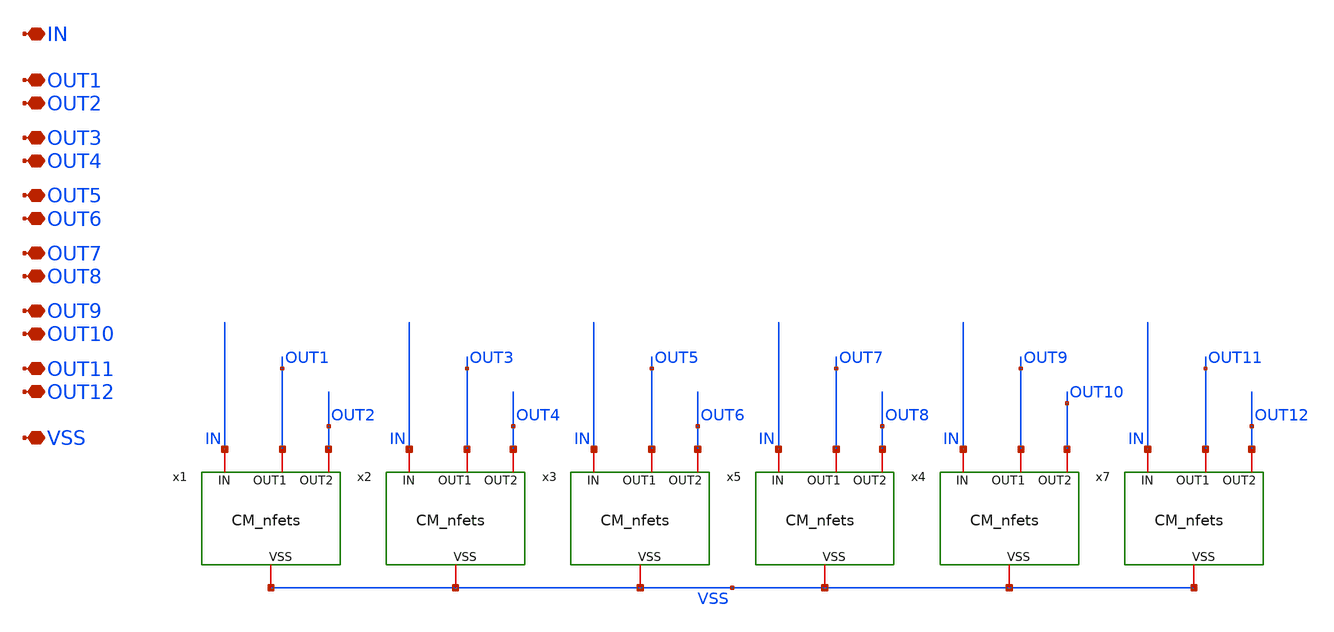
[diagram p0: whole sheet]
** sch_path: TIA_Filter/CurrentMirrors/CM_n_net.sch
**.subckt CM_n_net IN OUT1 OUT2 VSS OUT3 OUT4 OUT5 OUT6 OUT7 OUT8 OUT9 OUT10 OUT11 OUT12
*.iopin IN
*.iopin OUT1
*.iopin OUT2
*.iopin VSS
*.iopin OUT3
*.iopin OUT4
*.iopin OUT5
*.iopin OUT6
*.iopin OUT7
*.iopin OUT8
*.iopin OUT9
*.iopin OUT10
*.iopin OUT11
*.iopin OUT12
x1 IN OUT1 OUT2 VSS CM_nfets
x2 IN OUT3 OUT4 VSS CM_nfets
x4 IN OUT9 OUT10 VSS CM_nfets
x5 IN OUT7 OUT8 VSS CM_nfets
x3 IN OUT5 OUT6 VSS CM_nfets
x7 IN OUT11 OUT12 VSS CM_nfets
**.ends

* expanding   symbol:  CurrentMirrors/CM_nfets.sym # of pins=4
** sym_path: TIA_Filter/CurrentMirrors/CM_nfets.sym
** sch_path: TIA_Filter/CurrentMirrors/CM_nfets.sch
.subckt CM_nfets IN OUT1 OUT2 VSS
*.iopin IN
*.iopin OUT1
*.iopin OUT2
*.iopin VSS
XM2[1] IN IN VSS VSS nfet_03v3 L=2u W=2u nf=1 ad='int((nf+1)/2) * W/nf * 0.18u' as='int((nf+2)/2) * W/nf * 0.18u'
+ pd='2*int((nf+1)/2) * (W/nf + 0.18u)' ps='2*int((nf+2)/2) * (W/nf + 0.18u)' nrd='0.18u / W' nrs='0.18u / W'
+ sa=0 sb=0 sd=0 m=1
XM2[2] IN IN VSS VSS nfet_03v3 L=2u W=2u nf=1 ad='int((nf+1)/2) * W/nf * 0.18u' as='int((nf+2)/2) * W/nf * 0.18u'
+ pd='2*int((nf+1)/2) * (W/nf + 0.18u)' ps='2*int((nf+2)/2) * (W/nf + 0.18u)' nrd='0.18u / W' nrs='0.18u / W'
+ sa=0 sb=0 sd=0 m=1
XM2[3] IN IN VSS VSS nfet_03v3 L=2u W=2u nf=1 ad='int((nf+1)/2) * W/nf * 0.18u' as='int((nf+2)/2) * W/nf * 0.18u'
+ pd='2*int((nf+1)/2) * (W/nf + 0.18u)' ps='2*int((nf+2)/2) * (W/nf + 0.18u)' nrd='0.18u / W' nrs='0.18u / W'
+ sa=0 sb=0 sd=0 m=1
XM2[4] IN IN VSS VSS nfet_03v3 L=2u W=2u nf=1 ad='int((nf+1)/2) * W/nf * 0.18u' as='int((nf+2)/2) * W/nf * 0.18u'
+ pd='2*int((nf+1)/2) * (W/nf + 0.18u)' ps='2*int((nf+2)/2) * (W/nf + 0.18u)' nrd='0.18u / W' nrs='0.18u / W'
+ sa=0 sb=0 sd=0 m=1
XM2[5] IN IN VSS VSS nfet_03v3 L=2u W=2u nf=1 ad='int((nf+1)/2) * W/nf * 0.18u' as='int((nf+2)/2) * W/nf * 0.18u'
+ pd='2*int((nf+1)/2) * (W/nf + 0.18u)' ps='2*int((nf+2)/2) * (W/nf + 0.18u)' nrd='0.18u / W' nrs='0.18u / W'
+ sa=0 sb=0 sd=0 m=1
XM2[6] IN IN VSS VSS nfet_03v3 L=2u W=2u nf=1 ad='int((nf+1)/2) * W/nf * 0.18u' as='int((nf+2)/2) * W/nf * 0.18u'
+ pd='2*int((nf+1)/2) * (W/nf + 0.18u)' ps='2*int((nf+2)/2) * (W/nf + 0.18u)' nrd='0.18u / W' nrs='0.18u / W'
+ sa=0 sb=0 sd=0 m=1
XM2 OUT1 IN net3 VSS nfet_03v3 L=2u W=2u nf=1 ad='int((nf+1)/2) * W/nf * 0.18u' as='int((nf+2)/2) * W/nf * 0.18u'
+ pd='2*int((nf+1)/2) * (W/nf + 0.18u)' ps='2*int((nf+2)/2) * (W/nf + 0.18u)' nrd='0.18u / W' nrs='0.18u / W'
+ sa=0 sb=0 sd=0 m=1
XM11 net4 IN net6 VSS nfet_03v3 L=2u W=2u nf=1 ad='int((nf+1)/2) * W/nf * 0.18u' as='int((nf+2)/2) * W/nf * 0.18u'
+ pd='2*int((nf+1)/2) * (W/nf + 0.18u)' ps='2*int((nf+2)/2) * (W/nf + 0.18u)' nrd='0.18u / W' nrs='0.18u / W'
+ sa=0 sb=0 sd=0 m=1
XM12 net6 IN net7 VSS nfet_03v3 L=2u W=2u nf=1 ad='int((nf+1)/2) * W/nf * 0.18u' as='int((nf+2)/2) * W/nf * 0.18u'
+ pd='2*int((nf+1)/2) * (W/nf + 0.18u)' ps='2*int((nf+2)/2) * (W/nf + 0.18u)' nrd='0.18u / W' nrs='0.18u / W'
+ sa=0 sb=0 sd=0 m=1
XM13 net7 IN net8 VSS nfet_03v3 L=2u W=2u nf=1 ad='int((nf+1)/2) * W/nf * 0.18u' as='int((nf+2)/2) * W/nf * 0.18u'
+ pd='2*int((nf+1)/2) * (W/nf + 0.18u)' ps='2*int((nf+2)/2) * (W/nf + 0.18u)' nrd='0.18u / W' nrs='0.18u / W'
+ sa=0 sb=0 sd=0 m=1
XM14 net8 IN net9 VSS nfet_03v3 L=2u W=2u nf=1 ad='int((nf+1)/2) * W/nf * 0.18u' as='int((nf+2)/2) * W/nf * 0.18u'
+ pd='2*int((nf+1)/2) * (W/nf + 0.18u)' ps='2*int((nf+2)/2) * (W/nf + 0.18u)' nrd='0.18u / W' nrs='0.18u / W'
+ sa=0 sb=0 sd=0 m=1
XM15 net9 IN net10 VSS nfet_03v3 L=2u W=2u nf=1 ad='int((nf+1)/2) * W/nf * 0.18u' as='int((nf+2)/2) * W/nf * 0.18u'
+ pd='2*int((nf+1)/2) * (W/nf + 0.18u)' ps='2*int((nf+2)/2) * (W/nf + 0.18u)' nrd='0.18u / W' nrs='0.18u / W'
+ sa=0 sb=0 sd=0 m=1
XM16 net10 IN net11 VSS nfet_03v3 L=2u W=2u nf=1 ad='int((nf+1)/2) * W/nf * 0.18u' as='int((nf+2)/2) * W/nf * 0.18u'
+ pd='2*int((nf+1)/2) * (W/nf + 0.18u)' ps='2*int((nf+2)/2) * (W/nf + 0.18u)' nrd='0.18u / W' nrs='0.18u / W'
+ sa=0 sb=0 sd=0 m=1
XM17 net11 IN net12 VSS nfet_03v3 L=2u W=2u nf=1 ad='int((nf+1)/2) * W/nf * 0.18u' as='int((nf+2)/2) * W/nf * 0.18u'
+ pd='2*int((nf+1)/2) * (W/nf + 0.18u)' ps='2*int((nf+2)/2) * (W/nf + 0.18u)' nrd='0.18u / W' nrs='0.18u / W'
+ sa=0 sb=0 sd=0 m=1
XM18 net12 IN net13 VSS nfet_03v3 L=2u W=2u nf=1 ad='int((nf+1)/2) * W/nf * 0.18u' as='int((nf+2)/2) * W/nf * 0.18u'
+ pd='2*int((nf+1)/2) * (W/nf + 0.18u)' ps='2*int((nf+2)/2) * (W/nf + 0.18u)' nrd='0.18u / W' nrs='0.18u / W'
+ sa=0 sb=0 sd=0 m=1
XM19 net13 IN net14 VSS nfet_03v3 L=2u W=2u nf=1 ad='int((nf+1)/2) * W/nf * 0.18u' as='int((nf+2)/2) * W/nf * 0.18u'
+ pd='2*int((nf+1)/2) * (W/nf + 0.18u)' ps='2*int((nf+2)/2) * (W/nf + 0.18u)' nrd='0.18u / W' nrs='0.18u / W'
+ sa=0 sb=0 sd=0 m=1
XM20 net14 IN net1 VSS nfet_03v3 L=2u W=2u nf=1 ad='int((nf+1)/2) * W/nf * 0.18u' as='int((nf+2)/2) * W/nf * 0.18u'
+ pd='2*int((nf+1)/2) * (W/nf + 0.18u)' ps='2*int((nf+2)/2) * (W/nf + 0.18u)' nrd='0.18u / W' nrs='0.18u / W'
+ sa=0 sb=0 sd=0 m=1
XM21 net1 IN net15 VSS nfet_03v3 L=2u W=2u nf=1 ad='int((nf+1)/2) * W/nf * 0.18u' as='int((nf+2)/2) * W/nf * 0.18u'
+ pd='2*int((nf+1)/2) * (W/nf + 0.18u)' ps='2*int((nf+2)/2) * (W/nf + 0.18u)' nrd='0.18u / W' nrs='0.18u / W'
+ sa=0 sb=0 sd=0 m=1
XM22 net15 IN net16 VSS nfet_03v3 L=2u W=2u nf=1 ad='int((nf+1)/2) * W/nf * 0.18u' as='int((nf+2)/2) * W/nf * 0.18u'
+ pd='2*int((nf+1)/2) * (W/nf + 0.18u)' ps='2*int((nf+2)/2) * (W/nf + 0.18u)' nrd='0.18u / W' nrs='0.18u / W'
+ sa=0 sb=0 sd=0 m=1
XM23 net16 IN net17 VSS nfet_03v3 L=2u W=2u nf=1 ad='int((nf+1)/2) * W/nf * 0.18u' as='int((nf+2)/2) * W/nf * 0.18u'
+ pd='2*int((nf+1)/2) * (W/nf + 0.18u)' ps='2*int((nf+2)/2) * (W/nf + 0.18u)' nrd='0.18u / W' nrs='0.18u / W'
+ sa=0 sb=0 sd=0 m=1
XM24 net17 IN net18 VSS nfet_03v3 L=2u W=2u nf=1 ad='int((nf+1)/2) * W/nf * 0.18u' as='int((nf+2)/2) * W/nf * 0.18u'
+ pd='2*int((nf+1)/2) * (W/nf + 0.18u)' ps='2*int((nf+2)/2) * (W/nf + 0.18u)' nrd='0.18u / W' nrs='0.18u / W'
+ sa=0 sb=0 sd=0 m=1
XM25 net18 IN net19 VSS nfet_03v3 L=2u W=2u nf=1 ad='int((nf+1)/2) * W/nf * 0.18u' as='int((nf+2)/2) * W/nf * 0.18u'
+ pd='2*int((nf+1)/2) * (W/nf + 0.18u)' ps='2*int((nf+2)/2) * (W/nf + 0.18u)' nrd='0.18u / W' nrs='0.18u / W'
+ sa=0 sb=0 sd=0 m=1
XM26 net19 IN net20 VSS nfet_03v3 L=2u W=2u nf=1 ad='int((nf+1)/2) * W/nf * 0.18u' as='int((nf+2)/2) * W/nf * 0.18u'
+ pd='2*int((nf+1)/2) * (W/nf + 0.18u)' ps='2*int((nf+2)/2) * (W/nf + 0.18u)' nrd='0.18u / W' nrs='0.18u / W'
+ sa=0 sb=0 sd=0 m=1
XM27 net20 IN net21 VSS nfet_03v3 L=2u W=2u nf=1 ad='int((nf+1)/2) * W/nf * 0.18u' as='int((nf+2)/2) * W/nf * 0.18u'
+ pd='2*int((nf+1)/2) * (W/nf + 0.18u)' ps='2*int((nf+2)/2) * (W/nf + 0.18u)' nrd='0.18u / W' nrs='0.18u / W'
+ sa=0 sb=0 sd=0 m=1
XM28 net21 IN net22 VSS nfet_03v3 L=2u W=2u nf=1 ad='int((nf+1)/2) * W/nf * 0.18u' as='int((nf+2)/2) * W/nf * 0.18u'
+ pd='2*int((nf+1)/2) * (W/nf + 0.18u)' ps='2*int((nf+2)/2) * (W/nf + 0.18u)' nrd='0.18u / W' nrs='0.18u / W'
+ sa=0 sb=0 sd=0 m=1
XM29 net22 IN net23 VSS nfet_03v3 L=2u W=2u nf=1 ad='int((nf+1)/2) * W/nf * 0.18u' as='int((nf+2)/2) * W/nf * 0.18u'
+ pd='2*int((nf+1)/2) * (W/nf + 0.18u)' ps='2*int((nf+2)/2) * (W/nf + 0.18u)' nrd='0.18u / W' nrs='0.18u / W'
+ sa=0 sb=0 sd=0 m=1
XM30 net23 IN net2 VSS nfet_03v3 L=2u W=2u nf=1 ad='int((nf+1)/2) * W/nf * 0.18u' as='int((nf+2)/2) * W/nf * 0.18u'
+ pd='2*int((nf+1)/2) * (W/nf + 0.18u)' ps='2*int((nf+2)/2) * (W/nf + 0.18u)' nrd='0.18u / W' nrs='0.18u / W'
+ sa=0 sb=0 sd=0 m=1
XM31 net2 IN net24 VSS nfet_03v3 L=2u W=2u nf=1 ad='int((nf+1)/2) * W/nf * 0.18u' as='int((nf+2)/2) * W/nf * 0.18u'
+ pd='2*int((nf+1)/2) * (W/nf + 0.18u)' ps='2*int((nf+2)/2) * (W/nf + 0.18u)' nrd='0.18u / W' nrs='0.18u / W'
+ sa=0 sb=0 sd=0 m=1
XM32 net24 IN net25 VSS nfet_03v3 L=2u W=2u nf=1 ad='int((nf+1)/2) * W/nf * 0.18u' as='int((nf+2)/2) * W/nf * 0.18u'
+ pd='2*int((nf+1)/2) * (W/nf + 0.18u)' ps='2*int((nf+2)/2) * (W/nf + 0.18u)' nrd='0.18u / W' nrs='0.18u / W'
+ sa=0 sb=0 sd=0 m=1
XM33 net25 IN net26 VSS nfet_03v3 L=2u W=2u nf=1 ad='int((nf+1)/2) * W/nf * 0.18u' as='int((nf+2)/2) * W/nf * 0.18u'
+ pd='2*int((nf+1)/2) * (W/nf + 0.18u)' ps='2*int((nf+2)/2) * (W/nf + 0.18u)' nrd='0.18u / W' nrs='0.18u / W'
+ sa=0 sb=0 sd=0 m=1
XM34 net26 IN net27 VSS nfet_03v3 L=2u W=2u nf=1 ad='int((nf+1)/2) * W/nf * 0.18u' as='int((nf+2)/2) * W/nf * 0.18u'
+ pd='2*int((nf+1)/2) * (W/nf + 0.18u)' ps='2*int((nf+2)/2) * (W/nf + 0.18u)' nrd='0.18u / W' nrs='0.18u / W'
+ sa=0 sb=0 sd=0 m=1
XM35 net27 IN net28 VSS nfet_03v3 L=2u W=2u nf=1 ad='int((nf+1)/2) * W/nf * 0.18u' as='int((nf+2)/2) * W/nf * 0.18u'
+ pd='2*int((nf+1)/2) * (W/nf + 0.18u)' ps='2*int((nf+2)/2) * (W/nf + 0.18u)' nrd='0.18u / W' nrs='0.18u / W'
+ sa=0 sb=0 sd=0 m=1
XM36 net28 IN net29 VSS nfet_03v3 L=2u W=2u nf=1 ad='int((nf+1)/2) * W/nf * 0.18u' as='int((nf+2)/2) * W/nf * 0.18u'
+ pd='2*int((nf+1)/2) * (W/nf + 0.18u)' ps='2*int((nf+2)/2) * (W/nf + 0.18u)' nrd='0.18u / W' nrs='0.18u / W'
+ sa=0 sb=0 sd=0 m=1
XM1 net29 IN net30 VSS nfet_03v3 L=2u W=2u nf=1 ad='int((nf+1)/2) * W/nf * 0.18u' as='int((nf+2)/2) * W/nf * 0.18u'
+ pd='2*int((nf+1)/2) * (W/nf + 0.18u)' ps='2*int((nf+2)/2) * (W/nf + 0.18u)' nrd='0.18u / W' nrs='0.18u / W'
+ sa=0 sb=0 sd=0 m=1
XM37 net30 IN net31 VSS nfet_03v3 L=2u W=2u nf=1 ad='int((nf+1)/2) * W/nf * 0.18u' as='int((nf+2)/2) * W/nf * 0.18u'
+ pd='2*int((nf+1)/2) * (W/nf + 0.18u)' ps='2*int((nf+2)/2) * (W/nf + 0.18u)' nrd='0.18u / W' nrs='0.18u / W'
+ sa=0 sb=0 sd=0 m=1
XM38 net31 IN net32 VSS nfet_03v3 L=2u W=2u nf=1 ad='int((nf+1)/2) * W/nf * 0.18u' as='int((nf+2)/2) * W/nf * 0.18u'
+ pd='2*int((nf+1)/2) * (W/nf + 0.18u)' ps='2*int((nf+2)/2) * (W/nf + 0.18u)' nrd='0.18u / W' nrs='0.18u / W'
+ sa=0 sb=0 sd=0 m=1
XM9 net32 IN VSS VSS nfet_03v3 L=2u W=2u nf=1 ad='int((nf+1)/2) * W/nf * 0.18u' as='int((nf+2)/2) * W/nf * 0.18u'
+ pd='2*int((nf+1)/2) * (W/nf + 0.18u)' ps='2*int((nf+2)/2) * (W/nf + 0.18u)' nrd='0.18u / W' nrs='0.18u / W'
+ sa=0 sb=0 sd=0 m=1
XM5 net3 IN net4 VSS nfet_03v3 L=2u W=2u nf=1 ad='int((nf+1)/2) * W/nf * 0.18u' as='int((nf+2)/2) * W/nf * 0.18u'
+ pd='2*int((nf+1)/2) * (W/nf + 0.18u)' ps='2*int((nf+2)/2) * (W/nf + 0.18u)' nrd='0.18u / W' nrs='0.18u / W'
+ sa=0 sb=0 sd=0 m=1
XM8 net5 IN net33 VSS nfet_03v3 L=2u W=2u nf=1 ad='int((nf+1)/2) * W/nf * 0.18u' as='int((nf+2)/2) * W/nf * 0.18u'
+ pd='2*int((nf+1)/2) * (W/nf + 0.18u)' ps='2*int((nf+2)/2) * (W/nf + 0.18u)' nrd='0.18u / W' nrs='0.18u / W'
+ sa=0 sb=0 sd=0 m=1
XM10 net33 IN net34 VSS nfet_03v3 L=2u W=2u nf=1 ad='int((nf+1)/2) * W/nf * 0.18u' as='int((nf+2)/2) * W/nf * 0.18u'
+ pd='2*int((nf+1)/2) * (W/nf + 0.18u)' ps='2*int((nf+2)/2) * (W/nf + 0.18u)' nrd='0.18u / W' nrs='0.18u / W'
+ sa=0 sb=0 sd=0 m=1
XM39 net34 IN net35 VSS nfet_03v3 L=2u W=2u nf=1 ad='int((nf+1)/2) * W/nf * 0.18u' as='int((nf+2)/2) * W/nf * 0.18u'
+ pd='2*int((nf+1)/2) * (W/nf + 0.18u)' ps='2*int((nf+2)/2) * (W/nf + 0.18u)' nrd='0.18u / W' nrs='0.18u / W'
+ sa=0 sb=0 sd=0 m=1
XM40 net35 IN net36 VSS nfet_03v3 L=2u W=2u nf=1 ad='int((nf+1)/2) * W/nf * 0.18u' as='int((nf+2)/2) * W/nf * 0.18u'
+ pd='2*int((nf+1)/2) * (W/nf + 0.18u)' ps='2*int((nf+2)/2) * (W/nf + 0.18u)' nrd='0.18u / W' nrs='0.18u / W'
+ sa=0 sb=0 sd=0 m=1
XM41 net36 IN net37 VSS nfet_03v3 L=2u W=2u nf=1 ad='int((nf+1)/2) * W/nf * 0.18u' as='int((nf+2)/2) * W/nf * 0.18u'
+ pd='2*int((nf+1)/2) * (W/nf + 0.18u)' ps='2*int((nf+2)/2) * (W/nf + 0.18u)' nrd='0.18u / W' nrs='0.18u / W'
+ sa=0 sb=0 sd=0 m=1
XM42 net37 IN net38 VSS nfet_03v3 L=2u W=2u nf=1 ad='int((nf+1)/2) * W/nf * 0.18u' as='int((nf+2)/2) * W/nf * 0.18u'
+ pd='2*int((nf+1)/2) * (W/nf + 0.18u)' ps='2*int((nf+2)/2) * (W/nf + 0.18u)' nrd='0.18u / W' nrs='0.18u / W'
+ sa=0 sb=0 sd=0 m=1
XM43 net38 IN net39 VSS nfet_03v3 L=2u W=2u nf=1 ad='int((nf+1)/2) * W/nf * 0.18u' as='int((nf+2)/2) * W/nf * 0.18u'
+ pd='2*int((nf+1)/2) * (W/nf + 0.18u)' ps='2*int((nf+2)/2) * (W/nf + 0.18u)' nrd='0.18u / W' nrs='0.18u / W'
+ sa=0 sb=0 sd=0 m=1
XM44 net39 IN net40 VSS nfet_03v3 L=2u W=2u nf=1 ad='int((nf+1)/2) * W/nf * 0.18u' as='int((nf+2)/2) * W/nf * 0.18u'
+ pd='2*int((nf+1)/2) * (W/nf + 0.18u)' ps='2*int((nf+2)/2) * (W/nf + 0.18u)' nrd='0.18u / W' nrs='0.18u / W'
+ sa=0 sb=0 sd=0 m=1
XM45 net40 IN net41 VSS nfet_03v3 L=2u W=2u nf=1 ad='int((nf+1)/2) * W/nf * 0.18u' as='int((nf+2)/2) * W/nf * 0.18u'
+ pd='2*int((nf+1)/2) * (W/nf + 0.18u)' ps='2*int((nf+2)/2) * (W/nf + 0.18u)' nrd='0.18u / W' nrs='0.18u / W'
+ sa=0 sb=0 sd=0 m=1
XM46 net41 IN VSS VSS nfet_03v3 L=2u W=2u nf=1 ad='int((nf+1)/2) * W/nf * 0.18u' as='int((nf+2)/2) * W/nf * 0.18u'
+ pd='2*int((nf+1)/2) * (W/nf + 0.18u)' ps='2*int((nf+2)/2) * (W/nf + 0.18u)' nrd='0.18u / W' nrs='0.18u / W'
+ sa=0 sb=0 sd=0 m=1
XM47 OUT2 IN net42 VSS nfet_03v3 L=2u W=2u nf=1 ad='int((nf+1)/2) * W/nf * 0.18u' as='int((nf+2)/2) * W/nf * 0.18u'
+ pd='2*int((nf+1)/2) * (W/nf + 0.18u)' ps='2*int((nf+2)/2) * (W/nf + 0.18u)' nrd='0.18u / W' nrs='0.18u / W'
+ sa=0 sb=0 sd=0 m=1
XM48 net42 IN net43 VSS nfet_03v3 L=2u W=2u nf=1 ad='int((nf+1)/2) * W/nf * 0.18u' as='int((nf+2)/2) * W/nf * 0.18u'
+ pd='2*int((nf+1)/2) * (W/nf + 0.18u)' ps='2*int((nf+2)/2) * (W/nf + 0.18u)' nrd='0.18u / W' nrs='0.18u / W'
+ sa=0 sb=0 sd=0 m=1
XM49 net43 IN net44 VSS nfet_03v3 L=2u W=2u nf=1 ad='int((nf+1)/2) * W/nf * 0.18u' as='int((nf+2)/2) * W/nf * 0.18u'
+ pd='2*int((nf+1)/2) * (W/nf + 0.18u)' ps='2*int((nf+2)/2) * (W/nf + 0.18u)' nrd='0.18u / W' nrs='0.18u / W'
+ sa=0 sb=0 sd=0 m=1
XM50 net44 IN net45 VSS nfet_03v3 L=2u W=2u nf=1 ad='int((nf+1)/2) * W/nf * 0.18u' as='int((nf+2)/2) * W/nf * 0.18u'
+ pd='2*int((nf+1)/2) * (W/nf + 0.18u)' ps='2*int((nf+2)/2) * (W/nf + 0.18u)' nrd='0.18u / W' nrs='0.18u / W'
+ sa=0 sb=0 sd=0 m=1
XM51 net45 IN net46 VSS nfet_03v3 L=2u W=2u nf=1 ad='int((nf+1)/2) * W/nf * 0.18u' as='int((nf+2)/2) * W/nf * 0.18u'
+ pd='2*int((nf+1)/2) * (W/nf + 0.18u)' ps='2*int((nf+2)/2) * (W/nf + 0.18u)' nrd='0.18u / W' nrs='0.18u / W'
+ sa=0 sb=0 sd=0 m=1
XM52 net46 IN net5 VSS nfet_03v3 L=2u W=2u nf=1 ad='int((nf+1)/2) * W/nf * 0.18u' as='int((nf+2)/2) * W/nf * 0.18u'
+ pd='2*int((nf+1)/2) * (W/nf + 0.18u)' ps='2*int((nf+2)/2) * (W/nf + 0.18u)' nrd='0.18u / W' nrs='0.18u / W'
+ sa=0 sb=0 sd=0 m=1
XM1[1] VSS VSS VSS VSS nfet_03v3 L=2u W=2u nf=1 ad='int((nf+1)/2) * W/nf * 0.18u' as='int((nf+2)/2) * W/nf * 0.18u'
+ pd='2*int((nf+1)/2) * (W/nf + 0.18u)' ps='2*int((nf+2)/2) * (W/nf + 0.18u)' nrd='0.18u / W' nrs='0.18u / W'
+ sa=0 sb=0 sd=0 m=1
XM1[2] VSS VSS VSS VSS nfet_03v3 L=2u W=2u nf=1 ad='int((nf+1)/2) * W/nf * 0.18u' as='int((nf+2)/2) * W/nf * 0.18u'
+ pd='2*int((nf+1)/2) * (W/nf + 0.18u)' ps='2*int((nf+2)/2) * (W/nf + 0.18u)' nrd='0.18u / W' nrs='0.18u / W'
+ sa=0 sb=0 sd=0 m=1
XM1[3] VSS VSS VSS VSS nfet_03v3 L=2u W=2u nf=1 ad='int((nf+1)/2) * W/nf * 0.18u' as='int((nf+2)/2) * W/nf * 0.18u'
+ pd='2*int((nf+1)/2) * (W/nf + 0.18u)' ps='2*int((nf+2)/2) * (W/nf + 0.18u)' nrd='0.18u / W' nrs='0.18u / W'
+ sa=0 sb=0 sd=0 m=1
XM1[4] VSS VSS VSS VSS nfet_03v3 L=2u W=2u nf=1 ad='int((nf+1)/2) * W/nf * 0.18u' as='int((nf+2)/2) * W/nf * 0.18u'
+ pd='2*int((nf+1)/2) * (W/nf + 0.18u)' ps='2*int((nf+2)/2) * (W/nf + 0.18u)' nrd='0.18u / W' nrs='0.18u / W'
+ sa=0 sb=0 sd=0 m=1
XM1[5] VSS VSS VSS VSS nfet_03v3 L=2u W=2u nf=1 ad='int((nf+1)/2) * W/nf * 0.18u' as='int((nf+2)/2) * W/nf * 0.18u'
+ pd='2*int((nf+1)/2) * (W/nf + 0.18u)' ps='2*int((nf+2)/2) * (W/nf + 0.18u)' nrd='0.18u / W' nrs='0.18u / W'
+ sa=0 sb=0 sd=0 m=1
XM1[6] VSS VSS VSS VSS nfet_03v3 L=2u W=2u nf=1 ad='int((nf+1)/2) * W/nf * 0.18u' as='int((nf+2)/2) * W/nf * 0.18u'
+ pd='2*int((nf+1)/2) * (W/nf + 0.18u)' ps='2*int((nf+2)/2) * (W/nf + 0.18u)' nrd='0.18u / W' nrs='0.18u / W'
+ sa=0 sb=0 sd=0 m=1
XM1[7] VSS VSS VSS VSS nfet_03v3 L=2u W=2u nf=1 ad='int((nf+1)/2) * W/nf * 0.18u' as='int((nf+2)/2) * W/nf * 0.18u'
+ pd='2*int((nf+1)/2) * (W/nf + 0.18u)' ps='2*int((nf+2)/2) * (W/nf + 0.18u)' nrd='0.18u / W' nrs='0.18u / W'
+ sa=0 sb=0 sd=0 m=1
XM1[8] VSS VSS VSS VSS nfet_03v3 L=2u W=2u nf=1 ad='int((nf+1)/2) * W/nf * 0.18u' as='int((nf+2)/2) * W/nf * 0.18u'
+ pd='2*int((nf+1)/2) * (W/nf + 0.18u)' ps='2*int((nf+2)/2) * (W/nf + 0.18u)' nrd='0.18u / W' nrs='0.18u / W'
+ sa=0 sb=0 sd=0 m=1
XM1[9] VSS VSS VSS VSS nfet_03v3 L=2u W=2u nf=1 ad='int((nf+1)/2) * W/nf * 0.18u' as='int((nf+2)/2) * W/nf * 0.18u'
+ pd='2*int((nf+1)/2) * (W/nf + 0.18u)' ps='2*int((nf+2)/2) * (W/nf + 0.18u)' nrd='0.18u / W' nrs='0.18u / W'
+ sa=0 sb=0 sd=0 m=1
XM1[10] VSS VSS VSS VSS nfet_03v3 L=2u W=2u nf=1 ad='int((nf+1)/2) * W/nf * 0.18u' as='int((nf+2)/2) * W/nf * 0.18u'
+ pd='2*int((nf+1)/2) * (W/nf + 0.18u)' ps='2*int((nf+2)/2) * (W/nf + 0.18u)' nrd='0.18u / W' nrs='0.18u / W'
+ sa=0 sb=0 sd=0 m=1
XM1[11] VSS VSS VSS VSS nfet_03v3 L=2u W=2u nf=1 ad='int((nf+1)/2) * W/nf * 0.18u' as='int((nf+2)/2) * W/nf * 0.18u'
+ pd='2*int((nf+1)/2) * (W/nf + 0.18u)' ps='2*int((nf+2)/2) * (W/nf + 0.18u)' nrd='0.18u / W' nrs='0.18u / W'
+ sa=0 sb=0 sd=0 m=1
XM1[12] VSS VSS VSS VSS nfet_03v3 L=2u W=2u nf=1 ad='int((nf+1)/2) * W/nf * 0.18u' as='int((nf+2)/2) * W/nf * 0.18u'
+ pd='2*int((nf+1)/2) * (W/nf + 0.18u)' ps='2*int((nf+2)/2) * (W/nf + 0.18u)' nrd='0.18u / W' nrs='0.18u / W'
+ sa=0 sb=0 sd=0 m=1
XM1[13] VSS VSS VSS VSS nfet_03v3 L=2u W=2u nf=1 ad='int((nf+1)/2) * W/nf * 0.18u' as='int((nf+2)/2) * W/nf * 0.18u'
+ pd='2*int((nf+1)/2) * (W/nf + 0.18u)' ps='2*int((nf+2)/2) * (W/nf + 0.18u)' nrd='0.18u / W' nrs='0.18u / W'
+ sa=0 sb=0 sd=0 m=1
XM1[14] VSS VSS VSS VSS nfet_03v3 L=2u W=2u nf=1 ad='int((nf+1)/2) * W/nf * 0.18u' as='int((nf+2)/2) * W/nf * 0.18u'
+ pd='2*int((nf+1)/2) * (W/nf + 0.18u)' ps='2*int((nf+2)/2) * (W/nf + 0.18u)' nrd='0.18u / W' nrs='0.18u / W'
+ sa=0 sb=0 sd=0 m=1
XM1[15] VSS VSS VSS VSS nfet_03v3 L=2u W=2u nf=1 ad='int((nf+1)/2) * W/nf * 0.18u' as='int((nf+2)/2) * W/nf * 0.18u'
+ pd='2*int((nf+1)/2) * (W/nf + 0.18u)' ps='2*int((nf+2)/2) * (W/nf + 0.18u)' nrd='0.18u / W' nrs='0.18u / W'
+ sa=0 sb=0 sd=0 m=1
XM1[16] VSS VSS VSS VSS nfet_03v3 L=2u W=2u nf=1 ad='int((nf+1)/2) * W/nf * 0.18u' as='int((nf+2)/2) * W/nf * 0.18u'
+ pd='2*int((nf+1)/2) * (W/nf + 0.18u)' ps='2*int((nf+2)/2) * (W/nf + 0.18u)' nrd='0.18u / W' nrs='0.18u / W'
+ sa=0 sb=0 sd=0 m=1
XM1[17] VSS VSS VSS VSS nfet_03v3 L=2u W=2u nf=1 ad='int((nf+1)/2) * W/nf * 0.18u' as='int((nf+2)/2) * W/nf * 0.18u'
+ pd='2*int((nf+1)/2) * (W/nf + 0.18u)' ps='2*int((nf+2)/2) * (W/nf + 0.18u)' nrd='0.18u / W' nrs='0.18u / W'
+ sa=0 sb=0 sd=0 m=1
XM1[18] VSS VSS VSS VSS nfet_03v3 L=2u W=2u nf=1 ad='int((nf+1)/2) * W/nf * 0.18u' as='int((nf+2)/2) * W/nf * 0.18u'
+ pd='2*int((nf+1)/2) * (W/nf + 0.18u)' ps='2*int((nf+2)/2) * (W/nf + 0.18u)' nrd='0.18u / W' nrs='0.18u / W'
+ sa=0 sb=0 sd=0 m=1
XM1[19] VSS VSS VSS VSS nfet_03v3 L=2u W=2u nf=1 ad='int((nf+1)/2) * W/nf * 0.18u' as='int((nf+2)/2) * W/nf * 0.18u'
+ pd='2*int((nf+1)/2) * (W/nf + 0.18u)' ps='2*int((nf+2)/2) * (W/nf + 0.18u)' nrd='0.18u / W' nrs='0.18u / W'
+ sa=0 sb=0 sd=0 m=1
XM1[20] VSS VSS VSS VSS nfet_03v3 L=2u W=2u nf=1 ad='int((nf+1)/2) * W/nf * 0.18u' as='int((nf+2)/2) * W/nf * 0.18u'
+ pd='2*int((nf+1)/2) * (W/nf + 0.18u)' ps='2*int((nf+2)/2) * (W/nf + 0.18u)' nrd='0.18u / W' nrs='0.18u / W'
+ sa=0 sb=0 sd=0 m=1
XM1[21] VSS VSS VSS VSS nfet_03v3 L=2u W=2u nf=1 ad='int((nf+1)/2) * W/nf * 0.18u' as='int((nf+2)/2) * W/nf * 0.18u'
+ pd='2*int((nf+1)/2) * (W/nf + 0.18u)' ps='2*int((nf+2)/2) * (W/nf + 0.18u)' nrd='0.18u / W' nrs='0.18u / W'
+ sa=0 sb=0 sd=0 m=1
XM1[22] VSS VSS VSS VSS nfet_03v3 L=2u W=2u nf=1 ad='int((nf+1)/2) * W/nf * 0.18u' as='int((nf+2)/2) * W/nf * 0.18u'
+ pd='2*int((nf+1)/2) * (W/nf + 0.18u)' ps='2*int((nf+2)/2) * (W/nf + 0.18u)' nrd='0.18u / W' nrs='0.18u / W'
+ sa=0 sb=0 sd=0 m=1
XM1[23] VSS VSS VSS VSS nfet_03v3 L=2u W=2u nf=1 ad='int((nf+1)/2) * W/nf * 0.18u' as='int((nf+2)/2) * W/nf * 0.18u'
+ pd='2*int((nf+1)/2) * (W/nf + 0.18u)' ps='2*int((nf+2)/2) * (W/nf + 0.18u)' nrd='0.18u / W' nrs='0.18u / W'
+ sa=0 sb=0 sd=0 m=1
XM1[24] VSS VSS VSS VSS nfet_03v3 L=2u W=2u nf=1 ad='int((nf+1)/2) * W/nf * 0.18u' as='int((nf+2)/2) * W/nf * 0.18u'
+ pd='2*int((nf+1)/2) * (W/nf + 0.18u)' ps='2*int((nf+2)/2) * (W/nf + 0.18u)' nrd='0.18u / W' nrs='0.18u / W'
+ sa=0 sb=0 sd=0 m=1
XM1[25] VSS VSS VSS VSS nfet_03v3 L=2u W=2u nf=1 ad='int((nf+1)/2) * W/nf * 0.18u' as='int((nf+2)/2) * W/nf * 0.18u'
+ pd='2*int((nf+1)/2) * (W/nf + 0.18u)' ps='2*int((nf+2)/2) * (W/nf + 0.18u)' nrd='0.18u / W' nrs='0.18u / W'
+ sa=0 sb=0 sd=0 m=1
XM1[26] VSS VSS VSS VSS nfet_03v3 L=2u W=2u nf=1 ad='int((nf+1)/2) * W/nf * 0.18u' as='int((nf+2)/2) * W/nf * 0.18u'
+ pd='2*int((nf+1)/2) * (W/nf + 0.18u)' ps='2*int((nf+2)/2) * (W/nf + 0.18u)' nrd='0.18u / W' nrs='0.18u / W'
+ sa=0 sb=0 sd=0 m=1
XM1[27] VSS VSS VSS VSS nfet_03v3 L=2u W=2u nf=1 ad='int((nf+1)/2) * W/nf * 0.18u' as='int((nf+2)/2) * W/nf * 0.18u'
+ pd='2*int((nf+1)/2) * (W/nf + 0.18u)' ps='2*int((nf+2)/2) * (W/nf + 0.18u)' nrd='0.18u / W' nrs='0.18u / W'
+ sa=0 sb=0 sd=0 m=1
XM1[28] VSS VSS VSS VSS nfet_03v3 L=2u W=2u nf=1 ad='int((nf+1)/2) * W/nf * 0.18u' as='int((nf+2)/2) * W/nf * 0.18u'
+ pd='2*int((nf+1)/2) * (W/nf + 0.18u)' ps='2*int((nf+2)/2) * (W/nf + 0.18u)' nrd='0.18u / W' nrs='0.18u / W'
+ sa=0 sb=0 sd=0 m=1
XM1[29] VSS VSS VSS VSS nfet_03v3 L=2u W=2u nf=1 ad='int((nf+1)/2) * W/nf * 0.18u' as='int((nf+2)/2) * W/nf * 0.18u'
+ pd='2*int((nf+1)/2) * (W/nf + 0.18u)' ps='2*int((nf+2)/2) * (W/nf + 0.18u)' nrd='0.18u / W' nrs='0.18u / W'
+ sa=0 sb=0 sd=0 m=1
XM1[30] VSS VSS VSS VSS nfet_03v3 L=2u W=2u nf=1 ad='int((nf+1)/2) * W/nf * 0.18u' as='int((nf+2)/2) * W/nf * 0.18u'
+ pd='2*int((nf+1)/2) * (W/nf + 0.18u)' ps='2*int((nf+2)/2) * (W/nf + 0.18u)' nrd='0.18u / W' nrs='0.18u / W'
+ sa=0 sb=0 sd=0 m=1
XM1[31] VSS VSS VSS VSS nfet_03v3 L=2u W=2u nf=1 ad='int((nf+1)/2) * W/nf * 0.18u' as='int((nf+2)/2) * W/nf * 0.18u'
+ pd='2*int((nf+1)/2) * (W/nf + 0.18u)' ps='2*int((nf+2)/2) * (W/nf + 0.18u)' nrd='0.18u / W' nrs='0.18u / W'
+ sa=0 sb=0 sd=0 m=1
XM1[32] VSS VSS VSS VSS nfet_03v3 L=2u W=2u nf=1 ad='int((nf+1)/2) * W/nf * 0.18u' as='int((nf+2)/2) * W/nf * 0.18u'
+ pd='2*int((nf+1)/2) * (W/nf + 0.18u)' ps='2*int((nf+2)/2) * (W/nf + 0.18u)' nrd='0.18u / W' nrs='0.18u / W'
+ sa=0 sb=0 sd=0 m=1
XM1[33] VSS VSS VSS VSS nfet_03v3 L=2u W=2u nf=1 ad='int((nf+1)/2) * W/nf * 0.18u' as='int((nf+2)/2) * W/nf * 0.18u'
+ pd='2*int((nf+1)/2) * (W/nf + 0.18u)' ps='2*int((nf+2)/2) * (W/nf + 0.18u)' nrd='0.18u / W' nrs='0.18u / W'
+ sa=0 sb=0 sd=0 m=1
XM1[34] VSS VSS VSS VSS nfet_03v3 L=2u W=2u nf=1 ad='int((nf+1)/2) * W/nf * 0.18u' as='int((nf+2)/2) * W/nf * 0.18u'
+ pd='2*int((nf+1)/2) * (W/nf + 0.18u)' ps='2*int((nf+2)/2) * (W/nf + 0.18u)' nrd='0.18u / W' nrs='0.18u / W'
+ sa=0 sb=0 sd=0 m=1
.ends

.end
